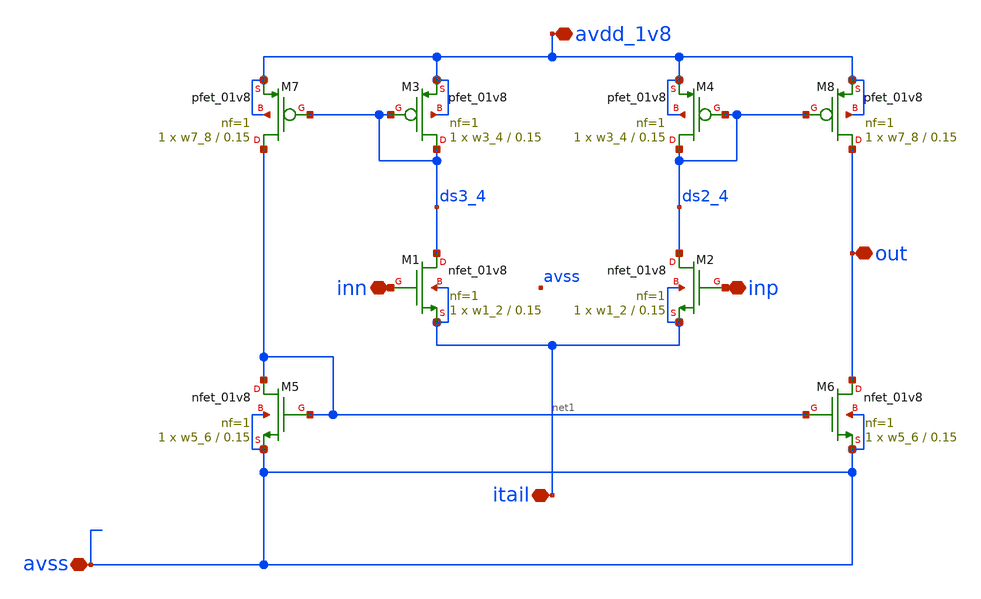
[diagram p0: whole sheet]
** sch_path: ISSCC25/submitted_notebooks/current_mirror_ota_optimization/characterization/sky130/schematics/cm_ota_rev1.sch
**.subckt cm_ota_rev1 inn inp out itail avss avdd_1v8
*.iopin inn
*.iopin inp
*.iopin out
*.iopin itail
*.iopin avss
*.iopin avdd_1v8
XM1 ds3_4 inn itail itail sky130_fd_pr__nfet_01v8 L=0.15 W=w1_2 nf=1 ad='int((nf+1)/2) * W/nf * 0.29'
+ as='int((nf+2)/2) * W/nf * 0.29' pd='2*int((nf+1)/2) * (W/nf + 0.29)' ps='2*int((nf+2)/2) * (W/nf + 0.29)'
+ nrd='0.29 / W' nrs='0.29 / W' sa=0 sb=0 sd=0 mult=1 m=1
xM3 ds3_4 ds3_4 avdd_1v8 avdd_1v8 sky130_fd_pr__pfet_01v8 L=0.15 W=w3_4 nf=1 ad='int((nf+1)/2) * W/nf * 0.29'
+ as='int((nf+2)/2) * W/nf * 0.29' pd='2*int((nf+1)/2) * (W/nf + 0.29)' ps='2*int((nf+2)/2) * (W/nf + 0.29)'
+ nrd='0.29 / W' nrs='0.29 / W' sa=0 sb=0 sd=0 mult=1 m=1
XM2 ds2_4 inp itail itail sky130_fd_pr__nfet_01v8 L=0.15 W=w1_2 nf=1 ad='int((nf+1)/2) * W/nf * 0.29'
+ as='int((nf+2)/2) * W/nf * 0.29' pd='2*int((nf+1)/2) * (W/nf + 0.29)' ps='2*int((nf+2)/2) * (W/nf + 0.29)'
+ nrd='0.29 / W' nrs='0.29 / W' sa=0 sb=0 sd=0 mult=1 m=1
xM4 ds2_4 ds2_4 avdd_1v8 avdd_1v8 sky130_fd_pr__pfet_01v8 L=0.15 W=w3_4 nf=1 ad='int((nf+1)/2) * W/nf * 0.29'
+ as='int((nf+2)/2) * W/nf * 0.29' pd='2*int((nf+1)/2) * (W/nf + 0.29)' ps='2*int((nf+2)/2) * (W/nf + 0.29)'
+ nrd='0.29 / W' nrs='0.29 / W' sa=0 sb=0 sd=0 mult=1 m=1
xM7 net1 ds3_4 avdd_1v8 avdd_1v8 sky130_fd_pr__pfet_01v8 L=0.15 W=w7_8 nf=1 ad='int((nf+1)/2) * W/nf * 0.29'
+ as='int((nf+2)/2) * W/nf * 0.29' pd='2*int((nf+1)/2) * (W/nf + 0.29)' ps='2*int((nf+2)/2) * (W/nf + 0.29)'
+ nrd='0.29 / W' nrs='0.29 / W' sa=0 sb=0 sd=0 mult=1 m=1
XM5 net1 net1 avss avss sky130_fd_pr__nfet_01v8 L=0.15 W=w5_6 nf=1 ad='int((nf+1)/2) * W/nf * 0.29' as='int((nf+2)/2) * W/nf * 0.29'
+ pd='2*int((nf+1)/2) * (W/nf + 0.29)' ps='2*int((nf+2)/2) * (W/nf + 0.29)' nrd='0.29 / W' nrs='0.29 / W'
+ sa=0 sb=0 sd=0 mult=1 m=1
XM6 out net1 avss avss sky130_fd_pr__nfet_01v8 L=0.15 W=w5_6 nf=1 ad='int((nf+1)/2) * W/nf * 0.29' as='int((nf+2)/2) * W/nf * 0.29'
+ pd='2*int((nf+1)/2) * (W/nf + 0.29)' ps='2*int((nf+2)/2) * (W/nf + 0.29)' nrd='0.29 / W' nrs='0.29 / W'
+ sa=0 sb=0 sd=0 mult=1 m=1
xM8 out ds2_4 avdd_1v8 avdd_1v8 sky130_fd_pr__pfet_01v8 L=0.15 W=w7_8 nf=1 ad='int((nf+1)/2) * W/nf * 0.29'
+ as='int((nf+2)/2) * W/nf * 0.29' pd='2*int((nf+1)/2) * (W/nf + 0.29)' ps='2*int((nf+2)/2) * (W/nf + 0.29)'
+ nrd='0.29 / W' nrs='0.29 / W' sa=0 sb=0 sd=0 mult=1 m=1
**.ends
.end
